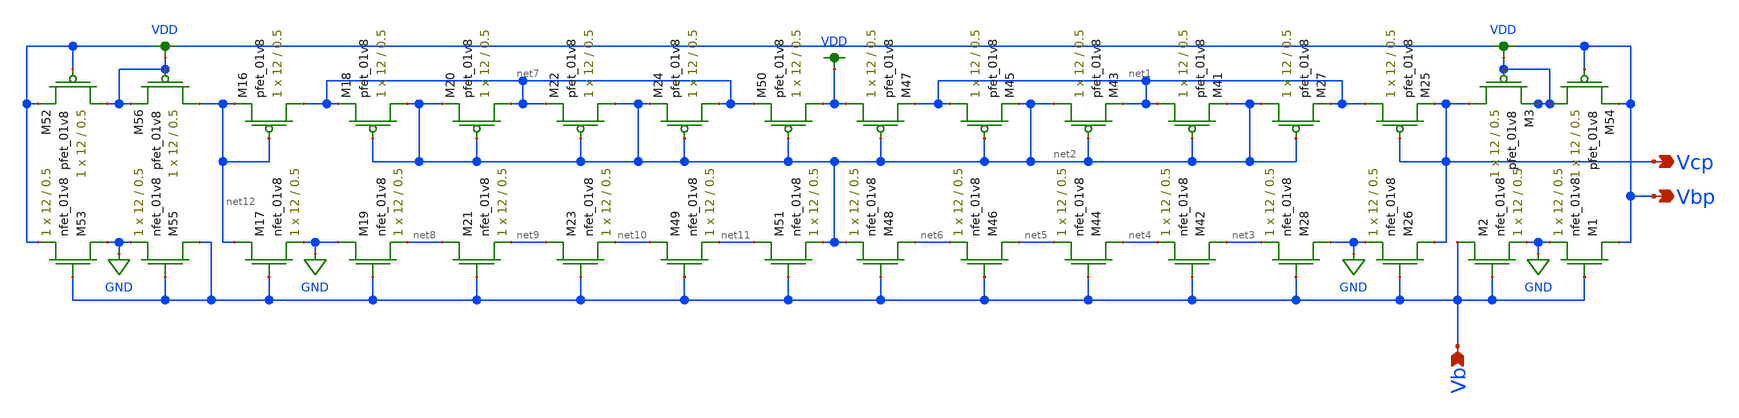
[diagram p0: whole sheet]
** sch_path: simulation/dac/v_gen_lds.sch
**.subckt v_gen_lds Vcp Vbp Vb
*.opin Vcp
*.opin Vbp
*.ipin Vb
XM25 net1 Vcp Vcp VDD sky130_fd_pr__pfet_01v8 L=0.5 W=12 nf=1 ad='int((nf+1)/2) * W/nf * 0.29' as='int((nf+2)/2) * W/nf * 0.29'
+ pd='2*int((nf+1)/2) * (W/nf + 0.29)' ps='2*int((nf+2)/2) * (W/nf + 0.29)' nrd='0.29 / W' nrs='0.29 / W'
+ sa=0 sb=0 sd=0 mult=1 m=1
XM26 Vcp Vb GND GND sky130_fd_pr__nfet_01v8 L=0.5 W=12 nf=1 ad='int((nf+1)/2) * W/nf * 0.29' as='int((nf+2)/2) * W/nf * 0.29'
+ pd='2*int((nf+1)/2) * (W/nf + 0.29)' ps='2*int((nf+2)/2) * (W/nf + 0.29)' nrd='0.29 / W' nrs='0.29 / W'
+ sa=0 sb=0 sd=0 mult=1 m=1
XM27 net2 net2 net1 VDD sky130_fd_pr__pfet_01v8 L=0.5 W=12 nf=1 ad='int((nf+1)/2) * W/nf * 0.29' as='int((nf+2)/2) * W/nf * 0.29'
+ pd='2*int((nf+1)/2) * (W/nf + 0.29)' ps='2*int((nf+2)/2) * (W/nf + 0.29)' nrd='0.29 / W' nrs='0.29 / W'
+ sa=0 sb=0 sd=0 mult=1 m=1
XM28 GND Vb net3 GND sky130_fd_pr__nfet_01v8 L=0.5 W=12 nf=1 ad='int((nf+1)/2) * W/nf * 0.29' as='int((nf+2)/2) * W/nf * 0.29'
+ pd='2*int((nf+1)/2) * (W/nf + 0.29)' ps='2*int((nf+2)/2) * (W/nf + 0.29)' nrd='0.29 / W' nrs='0.29 / W'
+ sa=0 sb=0 sd=0 mult=1 m=1
XM41 net1 net2 net2 VDD sky130_fd_pr__pfet_01v8 L=0.5 W=12 nf=1 ad='int((nf+1)/2) * W/nf * 0.29' as='int((nf+2)/2) * W/nf * 0.29'
+ pd='2*int((nf+1)/2) * (W/nf + 0.29)' ps='2*int((nf+2)/2) * (W/nf + 0.29)' nrd='0.29 / W' nrs='0.29 / W'
+ sa=0 sb=0 sd=0 mult=1 m=1
XM42 net3 Vb net4 GND sky130_fd_pr__nfet_01v8 L=0.5 W=12 nf=1 ad='int((nf+1)/2) * W/nf * 0.29' as='int((nf+2)/2) * W/nf * 0.29'
+ pd='2*int((nf+1)/2) * (W/nf + 0.29)' ps='2*int((nf+2)/2) * (W/nf + 0.29)' nrd='0.29 / W' nrs='0.29 / W'
+ sa=0 sb=0 sd=0 mult=1 m=1
XM43 net2 net2 net1 VDD sky130_fd_pr__pfet_01v8 L=0.5 W=12 nf=1 ad='int((nf+1)/2) * W/nf * 0.29' as='int((nf+2)/2) * W/nf * 0.29'
+ pd='2*int((nf+1)/2) * (W/nf + 0.29)' ps='2*int((nf+2)/2) * (W/nf + 0.29)' nrd='0.29 / W' nrs='0.29 / W'
+ sa=0 sb=0 sd=0 mult=1 m=1
XM44 net4 Vb net5 GND sky130_fd_pr__nfet_01v8 L=0.5 W=12 nf=1 ad='int((nf+1)/2) * W/nf * 0.29' as='int((nf+2)/2) * W/nf * 0.29'
+ pd='2*int((nf+1)/2) * (W/nf + 0.29)' ps='2*int((nf+2)/2) * (W/nf + 0.29)' nrd='0.29 / W' nrs='0.29 / W'
+ sa=0 sb=0 sd=0 mult=1 m=1
XM45 net1 net2 net2 VDD sky130_fd_pr__pfet_01v8 L=0.5 W=12 nf=1 ad='int((nf+1)/2) * W/nf * 0.29' as='int((nf+2)/2) * W/nf * 0.29'
+ pd='2*int((nf+1)/2) * (W/nf + 0.29)' ps='2*int((nf+2)/2) * (W/nf + 0.29)' nrd='0.29 / W' nrs='0.29 / W'
+ sa=0 sb=0 sd=0 mult=1 m=1
XM46 net5 Vb net6 GND sky130_fd_pr__nfet_01v8 L=0.5 W=12 nf=1 ad='int((nf+1)/2) * W/nf * 0.29' as='int((nf+2)/2) * W/nf * 0.29'
+ pd='2*int((nf+1)/2) * (W/nf + 0.29)' ps='2*int((nf+2)/2) * (W/nf + 0.29)' nrd='0.29 / W' nrs='0.29 / W'
+ sa=0 sb=0 sd=0 mult=1 m=1
XM47 VDD net2 net1 VDD sky130_fd_pr__pfet_01v8 L=0.5 W=12 nf=1 ad='int((nf+1)/2) * W/nf * 0.29' as='int((nf+2)/2) * W/nf * 0.29'
+ pd='2*int((nf+1)/2) * (W/nf + 0.29)' ps='2*int((nf+2)/2) * (W/nf + 0.29)' nrd='0.29 / W' nrs='0.29 / W'
+ sa=0 sb=0 sd=0 mult=1 m=1
XM48 net6 Vb net2 GND sky130_fd_pr__nfet_01v8 L=0.5 W=12 nf=1 ad='int((nf+1)/2) * W/nf * 0.29' as='int((nf+2)/2) * W/nf * 0.29'
+ pd='2*int((nf+1)/2) * (W/nf + 0.29)' ps='2*int((nf+2)/2) * (W/nf + 0.29)' nrd='0.29 / W' nrs='0.29 / W'
+ sa=0 sb=0 sd=0 mult=1 m=1
XM54 VDD Vbp Vbp VDD sky130_fd_pr__pfet_01v8 L=0.5 W=12 nf=1 ad='int((nf+1)/2) * W/nf * 0.29' as='int((nf+2)/2) * W/nf * 0.29'
+ pd='2*int((nf+1)/2) * (W/nf + 0.29)' ps='2*int((nf+2)/2) * (W/nf + 0.29)' nrd='0.29 / W' nrs='0.29 / W'
+ sa=0 sb=0 sd=0 mult=1 m=1
XM1 Vbp Vb GND GND sky130_fd_pr__nfet_01v8 L=0.5 W=12 nf=1 ad='int((nf+1)/2) * W/nf * 0.29' as='int((nf+2)/2) * W/nf * 0.29'
+ pd='2*int((nf+1)/2) * (W/nf + 0.29)' ps='2*int((nf+2)/2) * (W/nf + 0.29)' nrd='0.29 / W' nrs='0.29 / W'
+ sa=0 sb=0 sd=0 mult=1 m=1
XM2 Vb Vb GND GND sky130_fd_pr__nfet_01v8 L=0.5 W=12 nf=1 ad='int((nf+1)/2) * W/nf * 0.29' as='int((nf+2)/2) * W/nf * 0.29'
+ pd='2*int((nf+1)/2) * (W/nf + 0.29)' ps='2*int((nf+2)/2) * (W/nf + 0.29)' nrd='0.29 / W' nrs='0.29 / W'
+ sa=0 sb=0 sd=0 mult=1 m=1
XM3 Vcp VDD VDD VDD sky130_fd_pr__pfet_01v8 L=0.5 W=12 nf=1 ad='int((nf+1)/2) * W/nf * 0.29' as='int((nf+2)/2) * W/nf * 0.29'
+ pd='2*int((nf+1)/2) * (W/nf + 0.29)' ps='2*int((nf+2)/2) * (W/nf + 0.29)' nrd='0.29 / W' nrs='0.29 / W'
+ sa=0 sb=0 sd=0 mult=1 m=1
XM16 net7 net12 net12 VDD sky130_fd_pr__pfet_01v8 L=0.5 W=12 nf=1 ad='int((nf+1)/2) * W/nf * 0.29' as='int((nf+2)/2) * W/nf * 0.29'
+ pd='2*int((nf+1)/2) * (W/nf + 0.29)' ps='2*int((nf+2)/2) * (W/nf + 0.29)' nrd='0.29 / W' nrs='0.29 / W'
+ sa=0 sb=0 sd=0 mult=1 m=1
XM17 net12 Vb GND GND sky130_fd_pr__nfet_01v8 L=0.5 W=12 nf=1 ad='int((nf+1)/2) * W/nf * 0.29' as='int((nf+2)/2) * W/nf * 0.29'
+ pd='2*int((nf+1)/2) * (W/nf + 0.29)' ps='2*int((nf+2)/2) * (W/nf + 0.29)' nrd='0.29 / W' nrs='0.29 / W'
+ sa=0 sb=0 sd=0 mult=1 m=1
XM18 net2 net2 net7 VDD sky130_fd_pr__pfet_01v8 L=0.5 W=12 nf=1 ad='int((nf+1)/2) * W/nf * 0.29' as='int((nf+2)/2) * W/nf * 0.29'
+ pd='2*int((nf+1)/2) * (W/nf + 0.29)' ps='2*int((nf+2)/2) * (W/nf + 0.29)' nrd='0.29 / W' nrs='0.29 / W'
+ sa=0 sb=0 sd=0 mult=1 m=1
XM19 GND Vb net8 GND sky130_fd_pr__nfet_01v8 L=0.5 W=12 nf=1 ad='int((nf+1)/2) * W/nf * 0.29' as='int((nf+2)/2) * W/nf * 0.29'
+ pd='2*int((nf+1)/2) * (W/nf + 0.29)' ps='2*int((nf+2)/2) * (W/nf + 0.29)' nrd='0.29 / W' nrs='0.29 / W'
+ sa=0 sb=0 sd=0 mult=1 m=1
XM20 net7 net2 net2 VDD sky130_fd_pr__pfet_01v8 L=0.5 W=12 nf=1 ad='int((nf+1)/2) * W/nf * 0.29' as='int((nf+2)/2) * W/nf * 0.29'
+ pd='2*int((nf+1)/2) * (W/nf + 0.29)' ps='2*int((nf+2)/2) * (W/nf + 0.29)' nrd='0.29 / W' nrs='0.29 / W'
+ sa=0 sb=0 sd=0 mult=1 m=1
XM21 net8 Vb net9 GND sky130_fd_pr__nfet_01v8 L=0.5 W=12 nf=1 ad='int((nf+1)/2) * W/nf * 0.29' as='int((nf+2)/2) * W/nf * 0.29'
+ pd='2*int((nf+1)/2) * (W/nf + 0.29)' ps='2*int((nf+2)/2) * (W/nf + 0.29)' nrd='0.29 / W' nrs='0.29 / W'
+ sa=0 sb=0 sd=0 mult=1 m=1
XM22 net2 net2 net7 VDD sky130_fd_pr__pfet_01v8 L=0.5 W=12 nf=1 ad='int((nf+1)/2) * W/nf * 0.29' as='int((nf+2)/2) * W/nf * 0.29'
+ pd='2*int((nf+1)/2) * (W/nf + 0.29)' ps='2*int((nf+2)/2) * (W/nf + 0.29)' nrd='0.29 / W' nrs='0.29 / W'
+ sa=0 sb=0 sd=0 mult=1 m=1
XM23 net9 Vb net10 GND sky130_fd_pr__nfet_01v8 L=0.5 W=12 nf=1 ad='int((nf+1)/2) * W/nf * 0.29' as='int((nf+2)/2) * W/nf * 0.29'
+ pd='2*int((nf+1)/2) * (W/nf + 0.29)' ps='2*int((nf+2)/2) * (W/nf + 0.29)' nrd='0.29 / W' nrs='0.29 / W'
+ sa=0 sb=0 sd=0 mult=1 m=1
XM24 net7 net2 net2 VDD sky130_fd_pr__pfet_01v8 L=0.5 W=12 nf=1 ad='int((nf+1)/2) * W/nf * 0.29' as='int((nf+2)/2) * W/nf * 0.29'
+ pd='2*int((nf+1)/2) * (W/nf + 0.29)' ps='2*int((nf+2)/2) * (W/nf + 0.29)' nrd='0.29 / W' nrs='0.29 / W'
+ sa=0 sb=0 sd=0 mult=1 m=1
XM49 net10 Vb net11 GND sky130_fd_pr__nfet_01v8 L=0.5 W=12 nf=1 ad='int((nf+1)/2) * W/nf * 0.29' as='int((nf+2)/2) * W/nf * 0.29'
+ pd='2*int((nf+1)/2) * (W/nf + 0.29)' ps='2*int((nf+2)/2) * (W/nf + 0.29)' nrd='0.29 / W' nrs='0.29 / W'
+ sa=0 sb=0 sd=0 mult=1 m=1
XM50 VDD net2 net7 VDD sky130_fd_pr__pfet_01v8 L=0.5 W=12 nf=1 ad='int((nf+1)/2) * W/nf * 0.29' as='int((nf+2)/2) * W/nf * 0.29'
+ pd='2*int((nf+1)/2) * (W/nf + 0.29)' ps='2*int((nf+2)/2) * (W/nf + 0.29)' nrd='0.29 / W' nrs='0.29 / W'
+ sa=0 sb=0 sd=0 mult=1 m=1
XM51 net11 Vb net2 GND sky130_fd_pr__nfet_01v8 L=0.5 W=12 nf=1 ad='int((nf+1)/2) * W/nf * 0.29' as='int((nf+2)/2) * W/nf * 0.29'
+ pd='2*int((nf+1)/2) * (W/nf + 0.29)' ps='2*int((nf+2)/2) * (W/nf + 0.29)' nrd='0.29 / W' nrs='0.29 / W'
+ sa=0 sb=0 sd=0 mult=1 m=1
XM52 VDD Vbp Vbp VDD sky130_fd_pr__pfet_01v8 L=0.5 W=12 nf=1 ad='int((nf+1)/2) * W/nf * 0.29' as='int((nf+2)/2) * W/nf * 0.29'
+ pd='2*int((nf+1)/2) * (W/nf + 0.29)' ps='2*int((nf+2)/2) * (W/nf + 0.29)' nrd='0.29 / W' nrs='0.29 / W'
+ sa=0 sb=0 sd=0 mult=1 m=1
XM53 GND Vb Vbp GND sky130_fd_pr__nfet_01v8 L=0.5 W=12 nf=1 ad='int((nf+1)/2) * W/nf * 0.29' as='int((nf+2)/2) * W/nf * 0.29'
+ pd='2*int((nf+1)/2) * (W/nf + 0.29)' ps='2*int((nf+2)/2) * (W/nf + 0.29)' nrd='0.29 / W' nrs='0.29 / W'
+ sa=0 sb=0 sd=0 mult=1 m=1
XM55 Vb Vb GND GND sky130_fd_pr__nfet_01v8 L=0.5 W=12 nf=1 ad='int((nf+1)/2) * W/nf * 0.29' as='int((nf+2)/2) * W/nf * 0.29'
+ pd='2*int((nf+1)/2) * (W/nf + 0.29)' ps='2*int((nf+2)/2) * (W/nf + 0.29)' nrd='0.29 / W' nrs='0.29 / W'
+ sa=0 sb=0 sd=0 mult=1 m=1
XM56 net12 VDD VDD VDD sky130_fd_pr__pfet_01v8 L=0.5 W=12 nf=1 ad='int((nf+1)/2) * W/nf * 0.29' as='int((nf+2)/2) * W/nf * 0.29'
+ pd='2*int((nf+1)/2) * (W/nf + 0.29)' ps='2*int((nf+2)/2) * (W/nf + 0.29)' nrd='0.29 / W' nrs='0.29 / W'
+ sa=0 sb=0 sd=0 mult=1 m=1
**.ends
.GLOBAL GND
.GLOBAL VDD
.end
